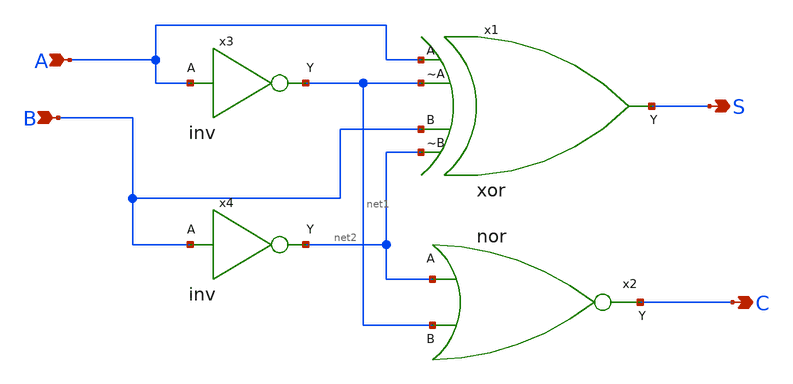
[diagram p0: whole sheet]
** sch_path: circuits/xschem/half_adder.sch
**.subckt half_adder A B S C
*.ipin A
*.ipin B
*.opin S
*.opin C
x1 B S A net1 net2 xor
x2 C net2 net1 nor
x4 net2 B inv
x3 net1 A inv
**.ends
.end
